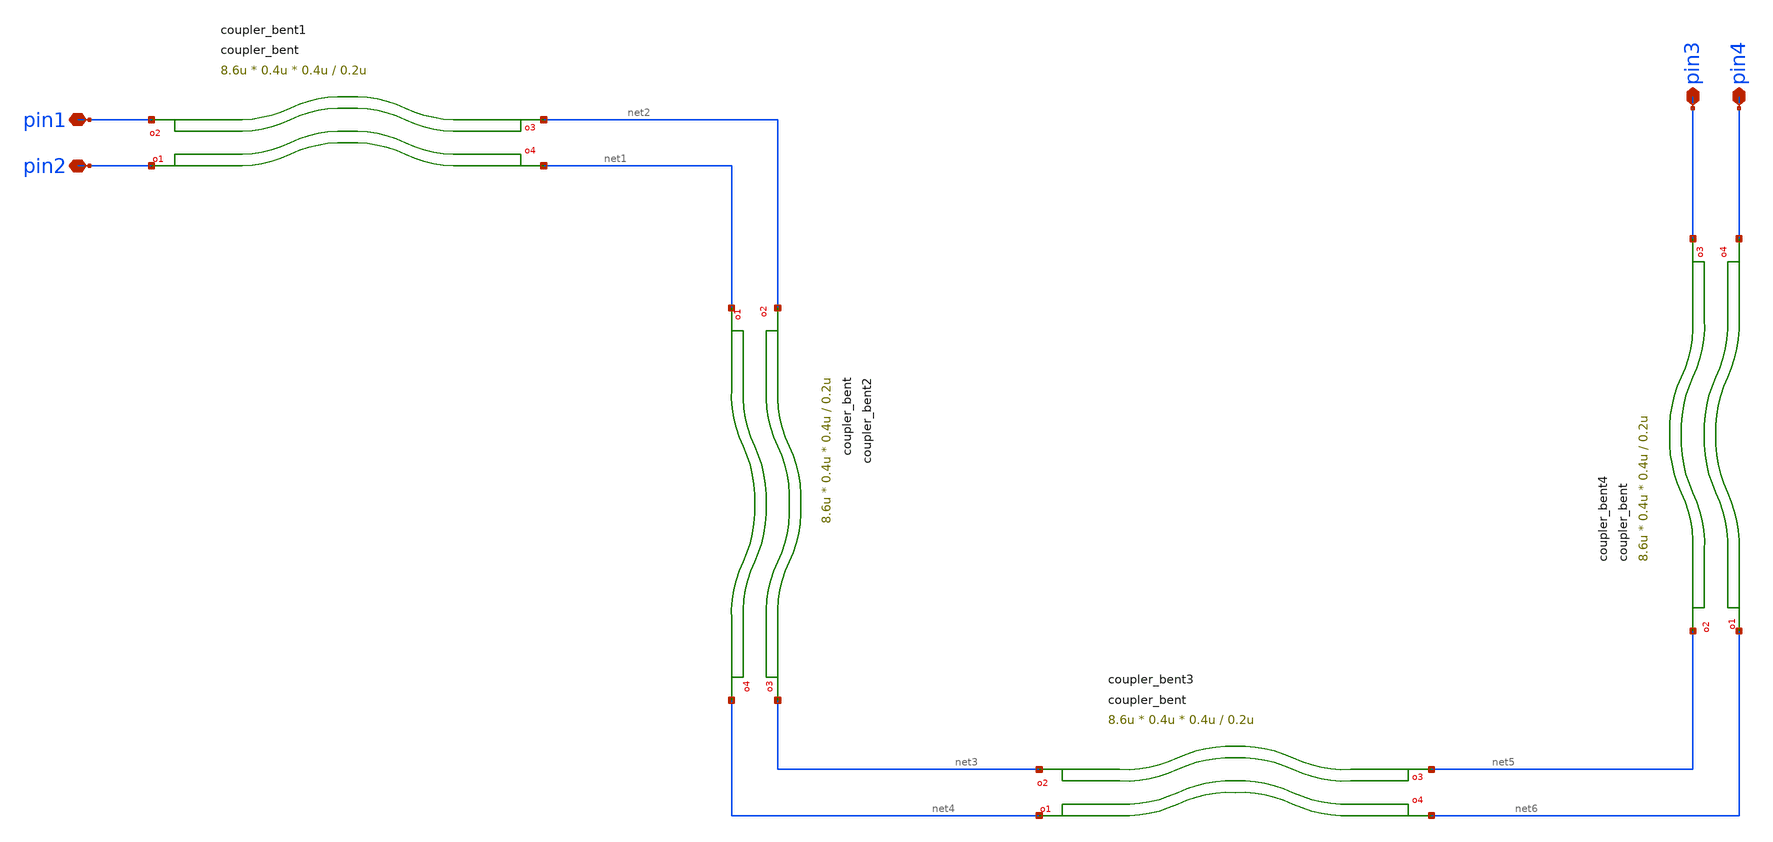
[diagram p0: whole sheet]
** sch_path: xschem/tests/test_sch/test_coupler_bent.sch
* Copyright (c) 2024, Mabrains LLC
* Licensed under the GNU Lesser General Public License, Version 3.0 (the "License");
* you may not use this file except in compliance with the License.
* GNU Lesser General Public License
* Version 3, 29 June 2007
* This program is free software: you can redistribute it and/or modify
* it under the terms of the GNU Lesser General Public License as published
* by the Free Software Foundation, either version 3 of the License, or
* (at your option) any later version.
* This program is distributed in the hope that it will be useful,
* but WITHOUT ANY WARRANTY; without even the implied warranty of
* MERCHANTABILITY or FITNESS FOR A PARTICULAR PURPOSE.  See the
* GNU Lesser General Public License for more details.
* You should have received a copy of the GNU Lesser General Public License
* along with this program.  If not, see <https://www.gnu.org/licenses/>.
* SPDX-License-Identifier: LGPL-3.0
**.subckt test_coupler_bent pin1 pin2 pin3 pin4
*.iopin pin1
*.iopin pin2
*.iopin pin3
*.iopin pin4
Pcoupler_bent1 pin1 pin2 net2 net1 coupler_bent gap=0.2u radius=26u length=8.6u width1=0.4u
+ width2=0.4u length_straight=10u
Pcoupler_bent3 net3 net4 net5 net6 coupler_bent gap=0.2u radius=26u length=8.6u width1=0.4u
+ width2=0.4u length_straight=10u
Pcoupler_bent4 net5 net6 pin3 pin4 coupler_bent gap=0.2u radius=26u length=8.6u width1=0.4u
+ width2=0.4u length_straight=10u
Pcoupler_bent2 net2 net1 net3 net4 coupler_bent gap=0.2u radius=26u length=8.6u width1=0.4u
+ width2=0.4u length_straight=10u
**.ends
.end
